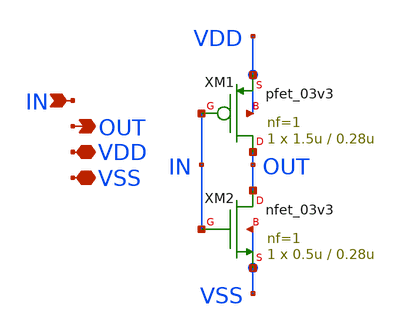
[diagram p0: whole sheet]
** sch_path: designs/libs/core_analog/inv_test/inv.sch
**.subckt inv IN OUT VDD VSS
*.ipin IN
*.opin OUT
*.iopin VDD
*.iopin VSS
XM1 OUT IN VDD VDD pfet_03v3 L=0.28u W=1.5u nf=1 ad='int((nf+1)/2) * W/nf * 0.18u' as='int((nf+2)/2) * W/nf * 0.18u'
+ pd='2*int((nf+1)/2) * (W/nf + 0.18u)' ps='2*int((nf+2)/2) * (W/nf + 0.18u)' nrd='0.18u / W' nrs='0.18u / W'
+ sa=0 sb=0 sd=0 m=1
XM2 OUT IN VSS VSS nfet_03v3 L=0.28u W=0.5u nf=1 ad='int((nf+1)/2) * W/nf * 0.18u' as='int((nf+2)/2) * W/nf * 0.18u'
+ pd='2*int((nf+1)/2) * (W/nf + 0.18u)' ps='2*int((nf+2)/2) * (W/nf + 0.18u)' nrd='0.18u / W' nrs='0.18u / W'
+ sa=0 sb=0 sd=0 m=1
**.ends
.end
